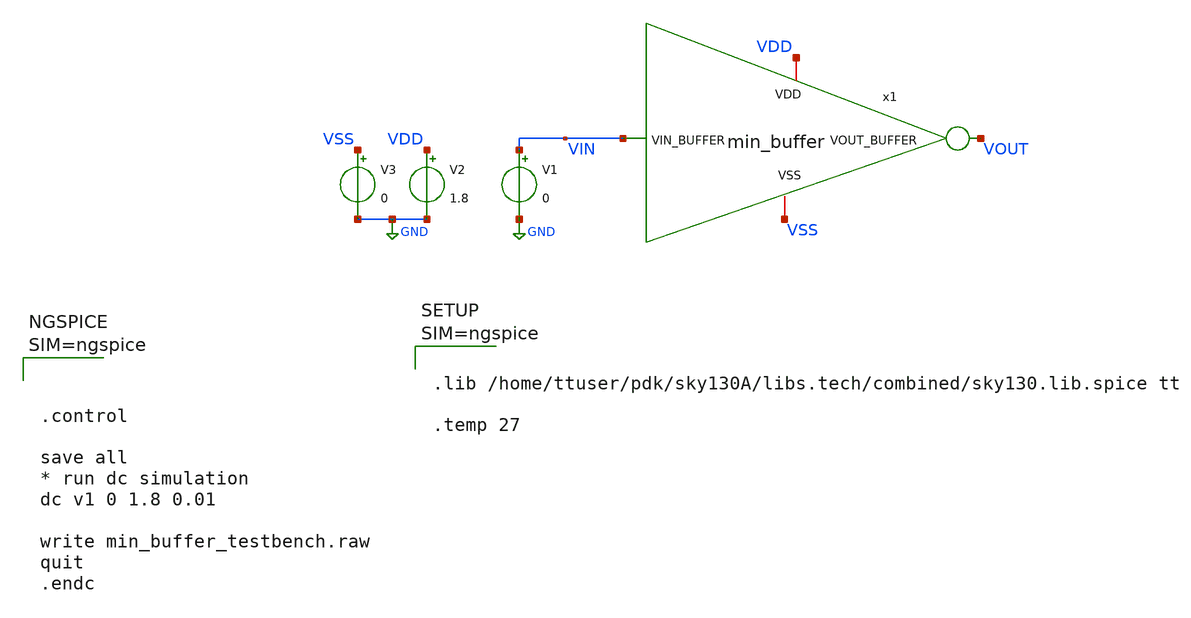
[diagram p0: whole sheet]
** sch_path: xschem/min_buffer_testbench.sch
**.subckt min_buffer_testbench
x1 VDD VSS VOUT VIN min_buffer
V1 VIN GND 0
V2 VDD GND 1.8
V3 VSS GND 0
**** begin user architecture code




.control

save all
* run dc simulation
dc v1 0 1.8 0.01

write min_buffer_testbench.raw
quit
.endc






.lib /home/ttuser/pdk/sky130A/libs.tech/combined/sky130.lib.spice tt

.temp 27



**** end user architecture code
**.ends

* expanding   symbol:  min_buffer.sym # of pins=4
** sym_path: xschem/min_buffer.sym
** sch_path: xschem/min_buffer.sch
.subckt min_buffer VDD VSS VOUT_BUFFER VIN_BUFFER
*.ipin VIN_BUFFER
*.opin VOUT_BUFFER
*.iopin VDD
*.iopin VSS
x1 VDD VSS VOUT_BUFFER INT_BUFFER min_inv
x2 VDD VSS INT_BUFFER VIN_BUFFER min_inv
.ends


* expanding   symbol:  min_inv.sym # of pins=4
** sym_path: xschem/min_inv.sym
** sch_path: xschem/min_inv.sch
.subckt min_inv VDD VSS VOUT_INV VIN_INV
*.iopin VDD
*.iopin VSS
*.ipin VIN_INV
*.opin VOUT_INV
XM2 VOUT_INV VIN_INV VSS VSS sky130_fd_pr__nfet_01v8 L=0.15 W=1 nf=1 ad='int((nf+1)/2) * W/nf * 0.29'
+ as='int((nf+2)/2) * W/nf * 0.29' pd='2*int((nf+1)/2) * (W/nf + 0.29)' ps='2*int((nf+2)/2) * (W/nf + 0.29)'
+ nrd='0.29 / W' nrs='0.29 / W' sa=0 sb=0 sd=0 mult=1 m=1
XM3 VOUT_INV VIN_INV VDD VDD sky130_fd_pr__pfet_01v8 L=0.15 W=1 nf=1 ad='int((nf+1)/2) * W/nf * 0.29'
+ as='int((nf+2)/2) * W/nf * 0.29' pd='2*int((nf+1)/2) * (W/nf + 0.29)' ps='2*int((nf+2)/2) * (W/nf + 0.29)'
+ nrd='0.29 / W' nrs='0.29 / W' sa=0 sb=0 sd=0 mult=1 m=1
.ends

.GLOBAL GND
.end
